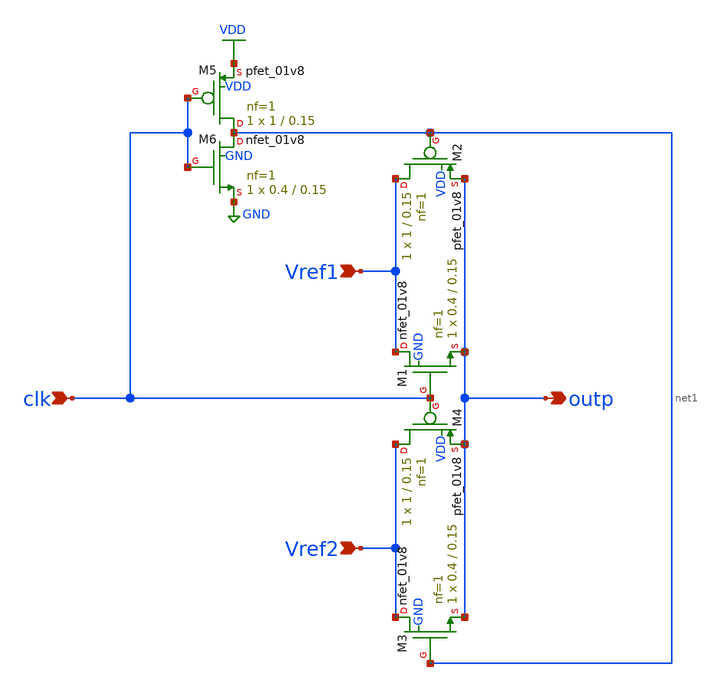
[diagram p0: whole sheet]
** sch_path: xschem/comparator/mux_working.sch
**.subckt mux_working Vref2 outp clk Vref1
*.ipin Vref2
*.opin outp
*.ipin clk
*.ipin Vref1
XM1 Vref1 clk outp GND sky130_fd_pr__nfet_01v8 L=0.15 W=0.4 nf=1 ad='int((nf+1)/2) * W/nf * 0.29' as='int((nf+2)/2) * W/nf * 0.29'
+ pd='2*int((nf+1)/2) * (W/nf + 0.29)' ps='2*int((nf+2)/2) * (W/nf + 0.29)' nrd='0.29 / W' nrs='0.29 / W'
+ sa=0 sb=0 sd=0 mult=1 m=1
XM2 Vref1 net1 outp VDD sky130_fd_pr__pfet_01v8 L=0.15 W=1 nf=1 ad='int((nf+1)/2) * W/nf * 0.29' as='int((nf+2)/2) * W/nf * 0.29'
+ pd='2*int((nf+1)/2) * (W/nf + 0.29)' ps='2*int((nf+2)/2) * (W/nf + 0.29)' nrd='0.29 / W' nrs='0.29 / W'
+ sa=0 sb=0 sd=0 mult=1 m=1
XM3 Vref2 net1 outp GND sky130_fd_pr__nfet_01v8 L=0.15 W=0.4 nf=1 ad='int((nf+1)/2) * W/nf * 0.29' as='int((nf+2)/2) * W/nf * 0.29'
+ pd='2*int((nf+1)/2) * (W/nf + 0.29)' ps='2*int((nf+2)/2) * (W/nf + 0.29)' nrd='0.29 / W' nrs='0.29 / W'
+ sa=0 sb=0 sd=0 mult=1 m=1
XM4 Vref2 clk outp VDD sky130_fd_pr__pfet_01v8 L=0.15 W=1 nf=1 ad='int((nf+1)/2) * W/nf * 0.29' as='int((nf+2)/2) * W/nf * 0.29'
+ pd='2*int((nf+1)/2) * (W/nf + 0.29)' ps='2*int((nf+2)/2) * (W/nf + 0.29)' nrd='0.29 / W' nrs='0.29 / W'
+ sa=0 sb=0 sd=0 mult=1 m=1
XM5 net1 clk VDD VDD sky130_fd_pr__pfet_01v8 L=0.15 W=1 nf=1 ad='int((nf+1)/2) * W/nf * 0.29' as='int((nf+2)/2) * W/nf * 0.29'
+ pd='2*int((nf+1)/2) * (W/nf + 0.29)' ps='2*int((nf+2)/2) * (W/nf + 0.29)' nrd='0.29 / W' nrs='0.29 / W'
+ sa=0 sb=0 sd=0 mult=1 m=1
XM6 net1 clk GND GND sky130_fd_pr__nfet_01v8 L=0.15 W=0.4 nf=1 ad='int((nf+1)/2) * W/nf * 0.29' as='int((nf+2)/2) * W/nf * 0.29'
+ pd='2*int((nf+1)/2) * (W/nf + 0.29)' ps='2*int((nf+2)/2) * (W/nf + 0.29)' nrd='0.29 / W' nrs='0.29 / W'
+ sa=0 sb=0 sd=0 mult=1 m=1
**.ends
.GLOBAL VDD
.GLOBAL GND
.end
